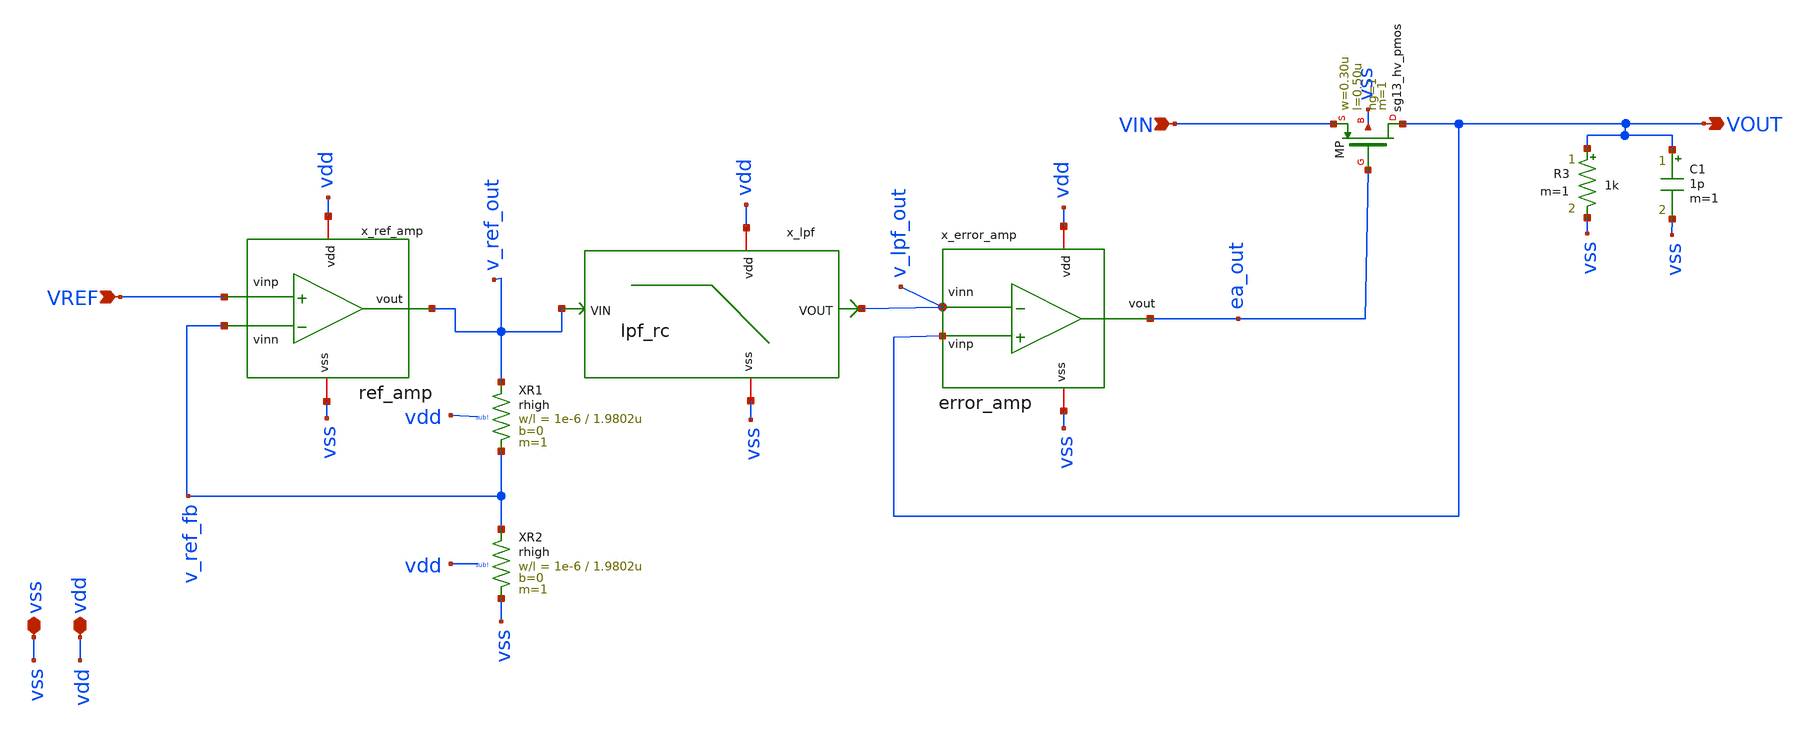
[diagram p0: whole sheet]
** sch_path: analog-db/drawings/ldo-005-ti-ldo-buffer-ref/ihp130/ldo/ldo_two_r.sch
**.subckt ldo_two_r VREF vdd vss VIN VOUT
*.ipin VREF
*.iopin vdd
*.iopin vss
*.ipin VIN
*.opin VOUT
x_ref_amp vdd v_ref_out VREF v_ref_fb vss ref_amp
XR1 v_ref_fb v_ref_out sub! rhigh w=1e-6 l=1.9802u m=1 b=0
XR2 vss v_ref_fb sub! rhigh w=1e-6 l=1.9802u m=1 b=0
x_error_amp vdd ea_out VOUT v_lpf_out vss error_amp
x_lpf net1 vss v_lpf_out v_ref_out lpf_rc
XMP VOUT ea_out VIN vss sg13_hv_pmos w=0.30u l=0.50u ng=1 m=1 mm_ok=1
R3 VOUT vss 1k m=1
C1 VOUT vss 1p m=1
**.ends
.end
